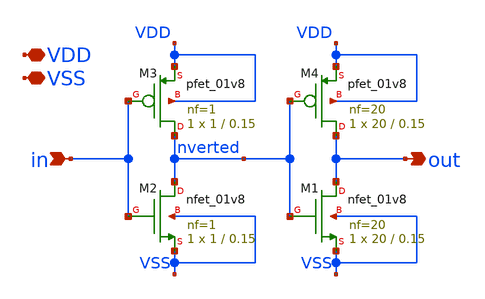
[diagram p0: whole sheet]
** sch_path: xschem/double_inverter.sch
**.subckt double_inverter VSS VDD in out
*.iopin VSS
*.iopin VDD
*.ipin in
*.opin out
XM2 inverted in VSS VSS sky130_fd_pr__nfet_01v8 L=0.15 W=1 nf=1 ad='int((nf+1)/2) * W/nf * 0.29' as='int((nf+2)/2) * W/nf * 0.29'
+ pd='2*int((nf+1)/2) * (W/nf + 0.29)' ps='2*int((nf+2)/2) * (W/nf + 0.29)' nrd='0.29 / W' nrs='0.29 / W'
+ sa=0 sb=0 sd=0 mult=1 m=1
XM3 inverted in VDD VDD sky130_fd_pr__pfet_01v8 L=0.15 W=1 nf=1 ad='int((nf+1)/2) * W/nf * 0.29' as='int((nf+2)/2) * W/nf * 0.29'
+ pd='2*int((nf+1)/2) * (W/nf + 0.29)' ps='2*int((nf+2)/2) * (W/nf + 0.29)' nrd='0.29 / W' nrs='0.29 / W'
+ sa=0 sb=0 sd=0 mult=1 m=1
XM1 out inverted VSS VSS sky130_fd_pr__nfet_01v8 L=0.15 W=20 nf=20 ad='int((nf+1)/2) * W/nf * 0.29' as='int((nf+2)/2) * W/nf * 0.29'
+ pd='2*int((nf+1)/2) * (W/nf + 0.29)' ps='2*int((nf+2)/2) * (W/nf + 0.29)' nrd='0.29 / W' nrs='0.29 / W'
+ sa=0 sb=0 sd=0 mult=1 m=1
XM4 out inverted VDD VDD sky130_fd_pr__pfet_01v8 L=0.15 W=20 nf=20 ad='int((nf+1)/2) * W/nf * 0.29' as='int((nf+2)/2) * W/nf * 0.29'
+ pd='2*int((nf+1)/2) * (W/nf + 0.29)' ps='2*int((nf+2)/2) * (W/nf + 0.29)' nrd='0.29 / W' nrs='0.29 / W'
+ sa=0 sb=0 sd=0 mult=1 m=1
**.ends
.end
